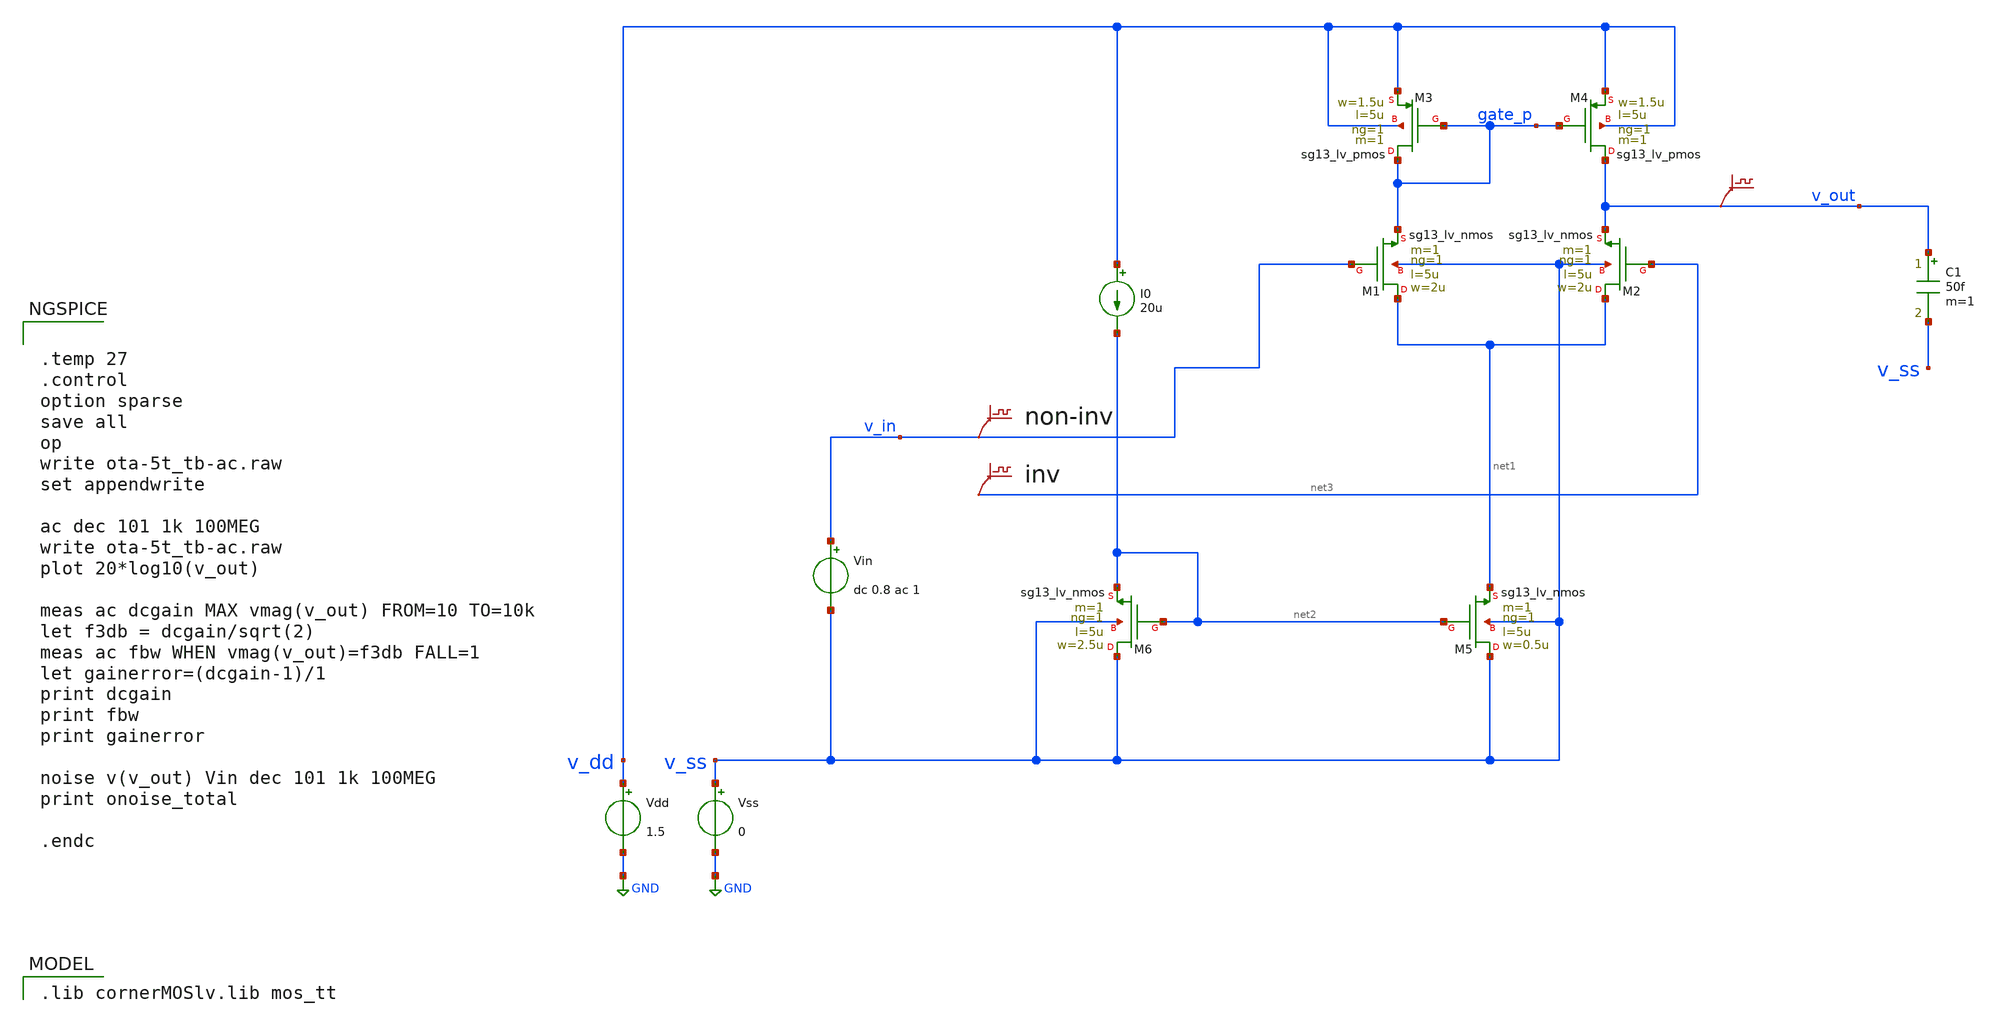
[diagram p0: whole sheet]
** sch_path: 3_Real_Cir/20_Real_Cir/ota-5t.sch
**.subckt ota-5t
Vdd v_dd GND 1.5
Vss v_ss GND 0
Vin v_in v_ss dc 0.8 ac 1
I0 v_dd net2 20u
.save v(v_in)
.save v(v_out)
C1 v_out v_ss 50f m=1
XM5 v_ss net2 net1 v_ss sg13_lv_nmos w=0.5u l=5u ng=1 m=1 mm_ok=1
XM4 v_out gate_p v_dd v_dd sg13_lv_pmos w=1.5u l=5u ng=1 m=1 mm_ok=1
XM1 net1 v_in gate_p v_ss sg13_lv_nmos w=2u l=5u ng=1 m=1 mm_ok=1
XM2 net1 net3 v_out v_ss sg13_lv_nmos w=2u l=5u ng=1 m=1 mm_ok=1
XM3 gate_p gate_p v_dd v_dd sg13_lv_pmos w=1.5u l=5u ng=1 m=1 mm_ok=1
XM6 v_ss net2 net2 v_ss sg13_lv_nmos w=2.5u l=5u ng=1 m=1 mm_ok=1
.save v(net3)
**** begin user architecture code
 .lib cornerMOSlv.lib mos_tt



.temp 27
.control
option sparse
save all
op
write ota-5t_tb-ac.raw
set appendwrite

ac dec 101 1k 100MEG
write ota-5t_tb-ac.raw
plot 20*log10(v_out)

meas ac dcgain MAX vmag(v_out) FROM=10 TO=10k
let f3db = dcgain/sqrt(2)
meas ac fbw WHEN vmag(v_out)=f3db FALL=1
let gainerror=(dcgain-1)/1
print dcgain
print fbw
print gainerror

noise v(v_out) Vin dec 101 1k 100MEG
print onoise_total

.endc


**** end user architecture code
**.ends
.GLOBAL GND
.end
